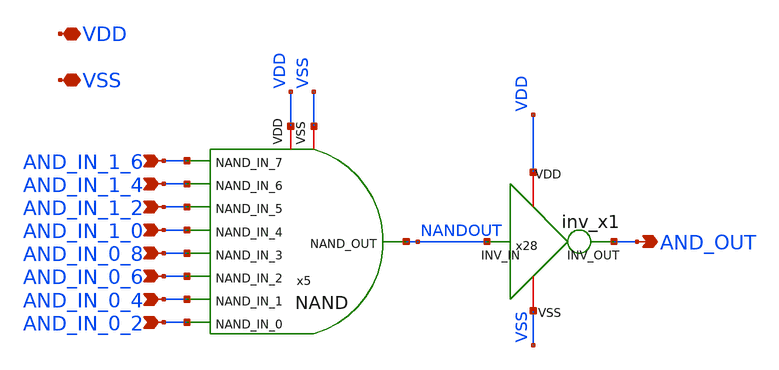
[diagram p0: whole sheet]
** sch_path: xschem/AND.sch
**.subckt AND VDD VSS AND_IN_0_2 AND_OUT AND_IN_0_4 AND_IN_0_6 AND_IN_0_8 AND_IN_1_0 AND_IN_1_2
*+ AND_IN_1_4 AND_IN_1_6
*.iopin VDD
*.iopin VSS
*.ipin AND_IN_0_2
*.opin AND_OUT
*.ipin AND_IN_0_4
*.ipin AND_IN_0_6
*.ipin AND_IN_0_8
*.ipin AND_IN_1_0
*.ipin AND_IN_1_2
*.ipin AND_IN_1_4
*.ipin AND_IN_1_6
x5 NANDOUT AND_IN_1_6 VDD AND_IN_1_4 VSS AND_IN_1_2 AND_IN_1_0 AND_IN_0_8 AND_IN_0_6 AND_IN_0_4
+ AND_IN_0_2 NAND
x28 VDD VSS AND_OUT NANDOUT inv_x1
**.ends
.end
